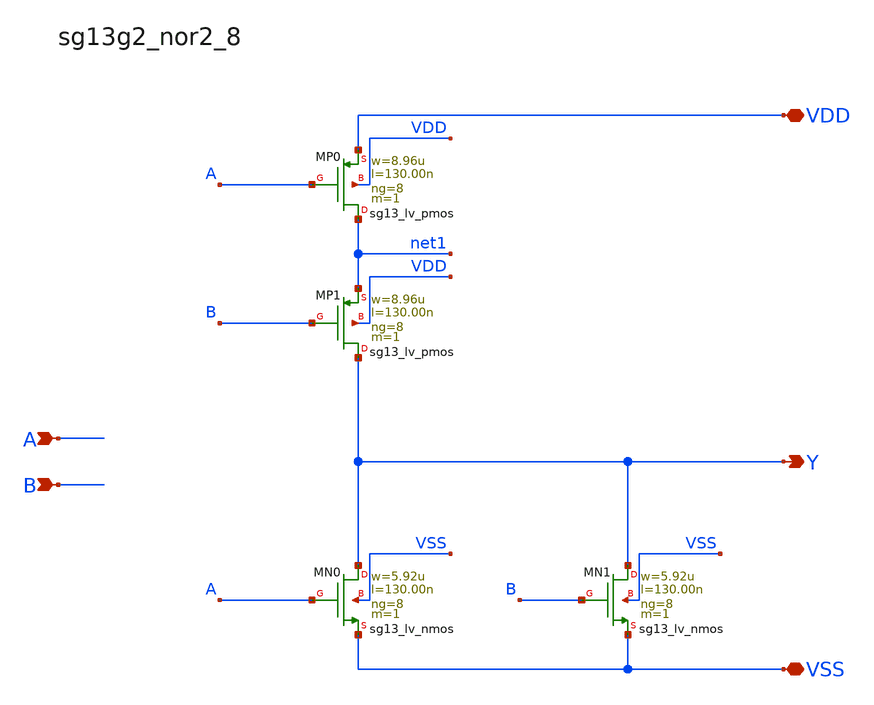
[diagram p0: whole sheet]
** sch_path: outputs/sg13g2_cells/cells/sg13g2_nor2_8/sg13g2_nor2_8.sch
**.subckt sg13g2_nor2_8 Y A B VDD VSS
*.opin Y
*.ipin A
*.ipin B
*.iopin VDD
*.iopin VSS
XMN0 Y A VSS VSS sg13_lv_nmos w=5.92u l=130.00n ng=8 m=1 mm_ok=1
XMN1 Y B VSS VSS sg13_lv_nmos w=5.92u l=130.00n ng=8 m=1 mm_ok=1
XMP0 net1 A VDD VDD sg13_lv_pmos w=8.96u l=130.00n ng=8 m=1 mm_ok=1
XMP1 Y B net1 VDD sg13_lv_pmos w=8.96u l=130.00n ng=8 m=1 mm_ok=1
**.ends
.end
